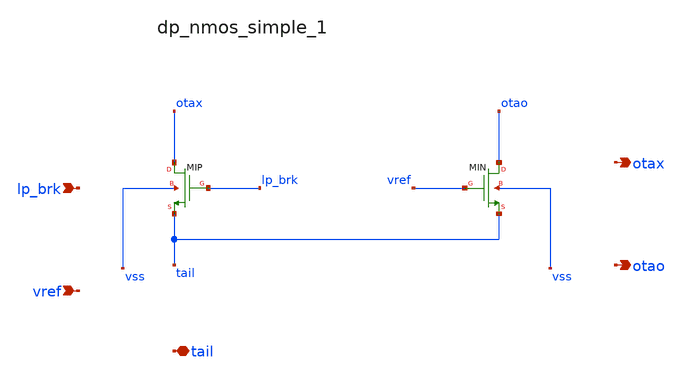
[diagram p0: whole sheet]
** sch_path: analog-db/raw/ldo_009_fer_5t_pass/hier/blocks/dp_nmos_simple_1.sch
**.subckt dp_nmos_simple_1 lp_brk vref tail otax otao
*.ipin lp_brk
*.ipin vref
*.iopin tail
*.opin otax
*.opin otao
XMIN otao vref tail vss sg13_lv_nmos w=x_dut_xmin_w l=x_dut_xmin_l ng=1 m=x_dut_xmin_m
XMIP otax lp_brk tail vss sg13_lv_nmos w=x_dut_xmip_w l=x_dut_xmip_l ng=1 m=x_dut_xmip_m
**.ends
.end
